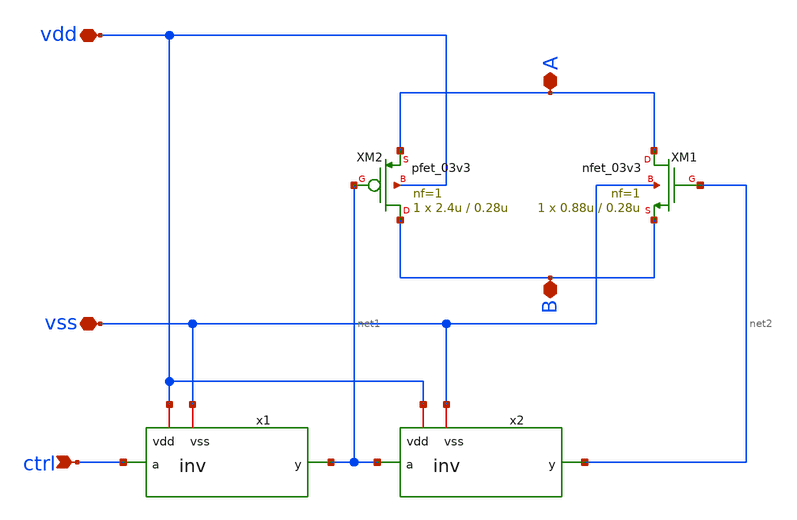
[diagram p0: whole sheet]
** sch_path: member_project/ice458/dynamic_comparator/xschem/cmos_sw.sch
**.subckt cmos_sw ctrl A B vdd vss
*.ipin ctrl
*.iopin A
*.iopin B
*.iopin vdd
*.iopin vss
x1 vdd ctrl net1 vss inv
x2 vdd net1 net2 vss inv
XM1 A net2 B vss nfet_03v3 L=0.28u W=0.88u nf=1 ad='int((nf+1)/2) * W/nf * 0.18u' as='int((nf+2)/2) * W/nf * 0.18u'
+ pd='2*int((nf+1)/2) * (W/nf + 0.18u)' ps='2*int((nf+2)/2) * (W/nf + 0.18u)' nrd='0.18u / W' nrs='0.18u / W'
+ sa=0 sb=0 sd=0 m=1
XM2 B net1 A vdd pfet_03v3 L=0.28u W=2.4u nf=1 ad='int((nf+1)/2) * W/nf * 0.18u' as='int((nf+2)/2) * W/nf * 0.18u'
+ pd='2*int((nf+1)/2) * (W/nf + 0.18u)' ps='2*int((nf+2)/2) * (W/nf + 0.18u)' nrd='0.18u / W' nrs='0.18u / W'
+ sa=0 sb=0 sd=0 m=1
**.ends

* expanding   symbol:  inv.sym # of pins=4
** sym_path: member_project/ice458/dynamic_comparator/xschem/inv.sym
** sch_path: member_project/ice458/dynamic_comparator/xschem/inv.sch
.subckt inv vdd a y vss
*.iopin vdd
*.iopin vss
*.ipin a
*.opin y
XM1 y a vss vss nfet_03v3 L=0.28u W=0.42u nf=1 ad='int((nf+1)/2) * W/nf * 0.18u' as='int((nf+2)/2) * W/nf * 0.18u'
+ pd='2*int((nf+1)/2) * (W/nf + 0.18u)' ps='2*int((nf+2)/2) * (W/nf + 0.18u)' nrd='0.18u / W' nrs='0.18u / W'
+ sa=0 sb=0 sd=0 m=1
XM2 y a vdd vdd pfet_03v3 L=0.28u W=1u nf=1 ad='int((nf+1)/2) * W/nf * 0.18u' as='int((nf+2)/2) * W/nf * 0.18u'
+ pd='2*int((nf+1)/2) * (W/nf + 0.18u)' ps='2*int((nf+2)/2) * (W/nf + 0.18u)' nrd='0.18u / W' nrs='0.18u / W'
+ sa=0 sb=0 sd=0 m=1
.ends

.end
